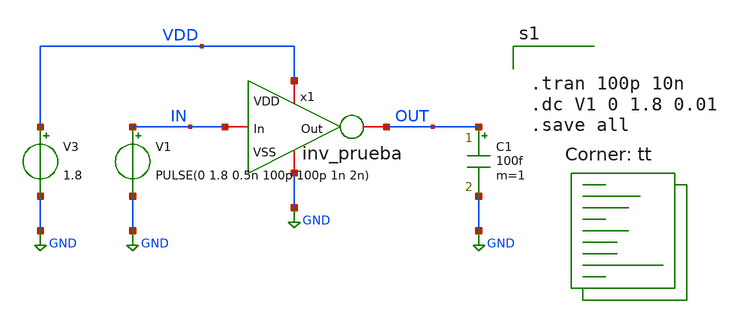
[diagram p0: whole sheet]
** sch_path: HVT/xschem_pruebas/tb_inv_prueba.sch
**.subckt tb_inv_prueba
x1 VDD OUT IN GND inv_prueba
V1 IN GND PULSE(0 1.8 0.5n 100p 100p 1n 2n)
C1 OUT GND 100f m=1
V3 VDD GND 1.8
**** begin user architecture code


.tran 100p 10n
.dc V1 0 1.8 0.01
.save all


.lib $::SKYWATER_MODELS/sky130.lib.spice tt
**** end user architecture code
**.ends

* expanding   symbol:  /foss/designs/xschem_pruebas/inv_prueba.sym # of pins=4
** sym_path: HVT/xschem_pruebas/inv_prueba.sym
** sch_path: HVT/xschem_pruebas/inv_prueba.sch
.subckt inv_prueba VDD Out In VSS
*.iopin Out
*.iopin In
*.iopin VDD
*.iopin VSS
XM3 Out In VDD VDD sky130_fd_pr__pfet_01v8 L=0.15 W=1 nf=1 ad='int((nf+1)/2) * W/nf * 0.29' as='int((nf+2)/2) * W/nf * 0.29'
+ pd='2*int((nf+1)/2) * (W/nf + 0.29)' ps='2*int((nf+2)/2) * (W/nf + 0.29)' nrd='0.29 / W' nrs='0.29 / W'
+ sa=0 sb=0 sd=0 mult=1 m=1
XM4 Out In VSS VSS sky130_fd_pr__nfet_01v8 L=0.15 W=1 nf=1 ad='int((nf+1)/2) * W/nf * 0.29' as='int((nf+2)/2) * W/nf * 0.29'
+ pd='2*int((nf+1)/2) * (W/nf + 0.29)' ps='2*int((nf+2)/2) * (W/nf + 0.29)' nrd='0.29 / W' nrs='0.29 / W'
+ sa=0 sb=0 sd=0 mult=1 m=1
.ends

.GLOBAL GND
.end
